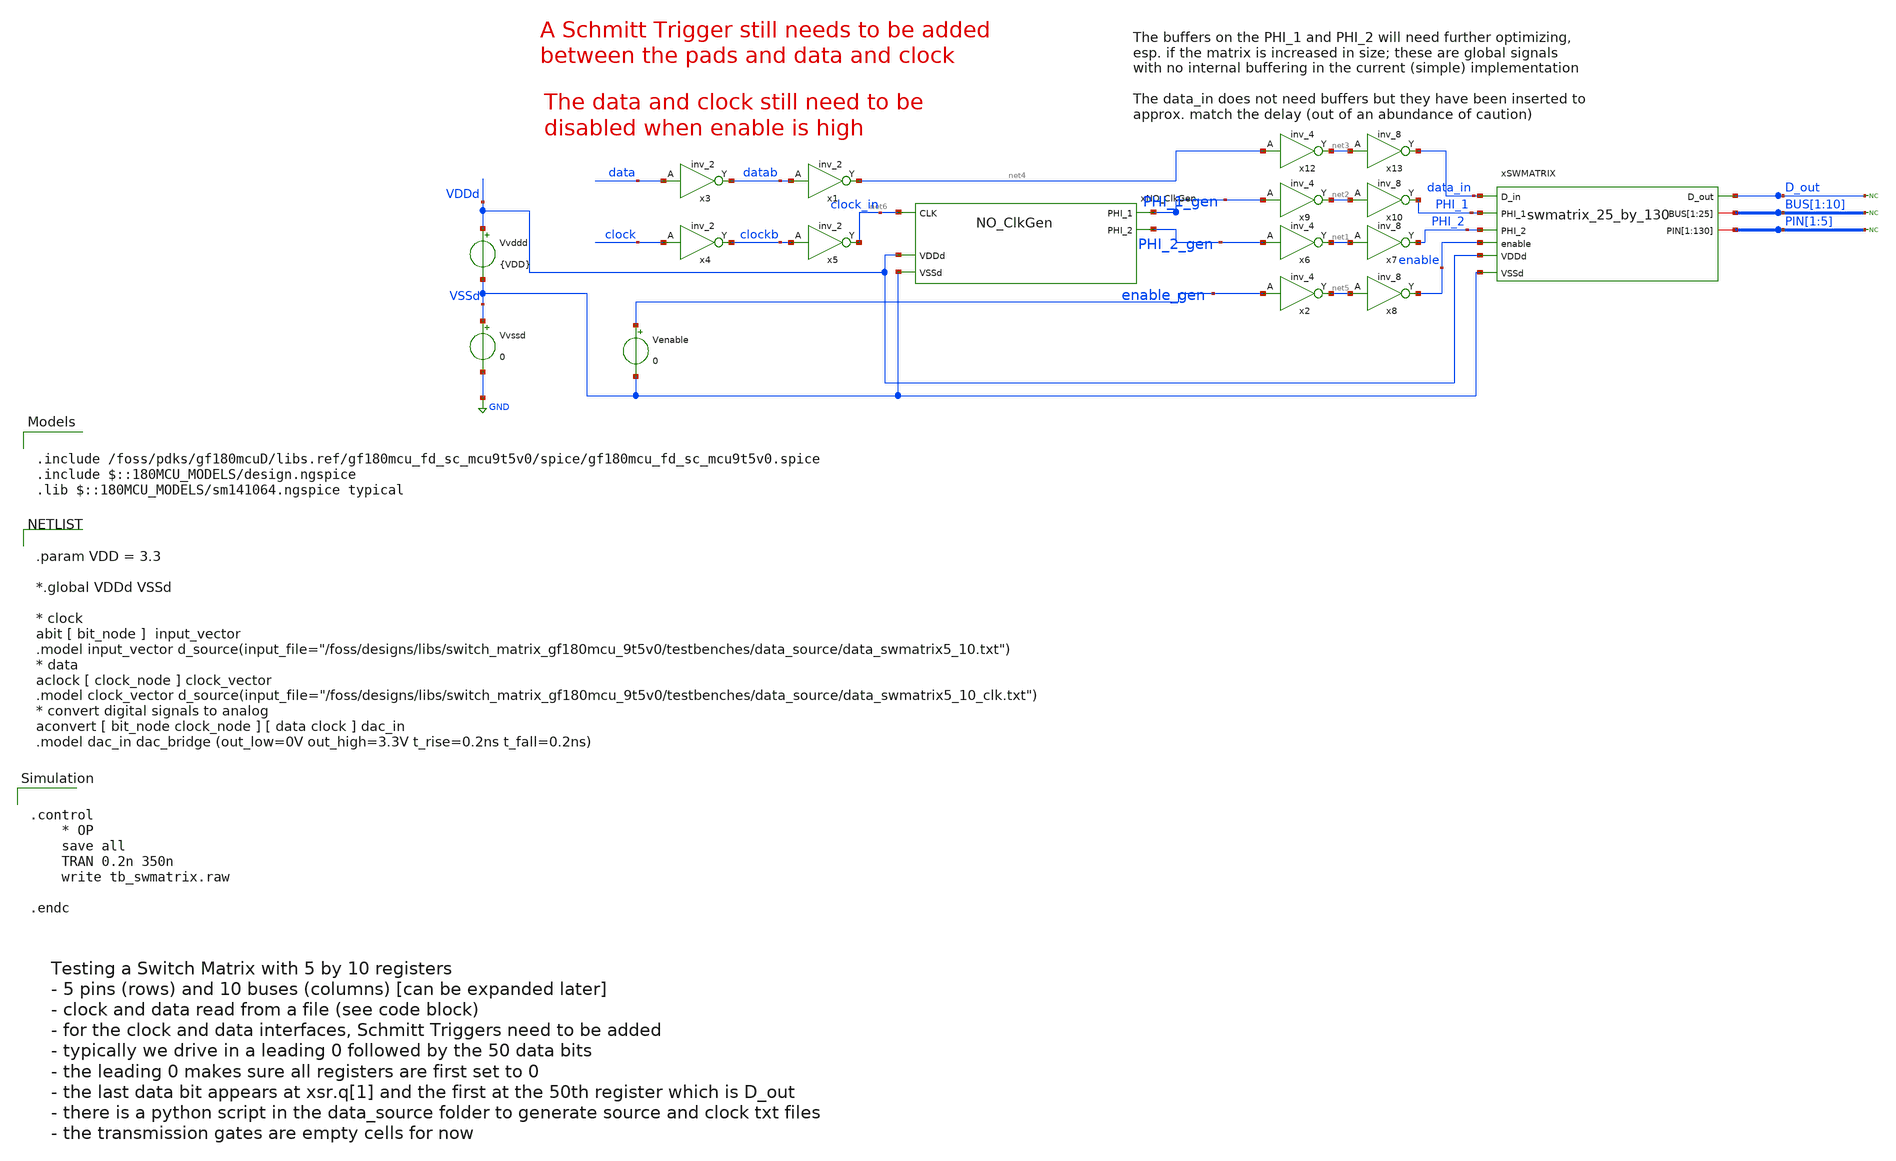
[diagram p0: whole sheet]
** sch_path: testbenches/tb_swmatrix_MOSbiusV3.sch
**.subckt tb_swmatrix_MOSbiusV3
Vvssd VSSd GND 0
Vvddd VDDd VSSd {VDD}
xNO_ClkGen PHI_2_gen net6 PHI_1_gen VDDd VSSd NO_ClkGen
x3 data VSSd VDDd VSSd VDDd datab gf180mcu_fd_sc_mcu9t5v0__inv_2
x1 datab VSSd VDDd VSSd VDDd net4 gf180mcu_fd_sc_mcu9t5v0__inv_2
x4 clock VSSd VDDd VSSd VDDd clockb gf180mcu_fd_sc_mcu9t5v0__inv_2
x5 clockb VSSd VDDd VSSd VDDd net6 gf180mcu_fd_sc_mcu9t5v0__inv_2
xSWMATRIX data_in D_out PHI_1 PHI_2 BUS[1] BUS[2] BUS[3] BUS[4] BUS[5] BUS[6] BUS[7] BUS[8] BUS[9]
+ BUS[10] BUS[1] BUS[2] BUS[3] BUS[4] BUS[5] BUS[6] BUS[7] BUS[8] BUS[9] BUS[10] BUS[1] BUS[2] BUS[3] BUS[4]
+ BUS[5] PIN[1] PIN[2] PIN[3] PIN[4] PIN[5] PIN[1] PIN[2] PIN[3] PIN[4] PIN[5] PIN[1] PIN[2] PIN[3] PIN[4]
+ PIN[5] PIN[1] PIN[2] PIN[3] PIN[4] PIN[5] PIN[1] PIN[2] PIN[3] PIN[4] PIN[5] PIN[1] PIN[2] PIN[3] PIN[4]
+ PIN[5] PIN[1] PIN[2] PIN[3] PIN[4] PIN[5] PIN[1] PIN[2] PIN[3] PIN[4] PIN[5] PIN[1] PIN[2] PIN[3] PIN[4]
+ PIN[5] PIN[1] PIN[2] PIN[3] PIN[4] PIN[5] PIN[1] PIN[2] PIN[3] PIN[4] PIN[5] PIN[1] PIN[2] PIN[3] PIN[4]
+ PIN[5] PIN[1] PIN[2] PIN[3] PIN[4] PIN[5] PIN[1] PIN[2] PIN[3] PIN[4] PIN[5] PIN[1] PIN[2] PIN[3] PIN[4]
+ PIN[5] PIN[1] PIN[2] PIN[3] PIN[4] PIN[5] PIN[1] PIN[2] PIN[3] PIN[4] PIN[5] PIN[1] PIN[2] PIN[3] PIN[4]
+ PIN[5] PIN[1] PIN[2] PIN[3] PIN[4] PIN[5] PIN[1] PIN[2] PIN[3] PIN[4] PIN[5] PIN[1] PIN[2] PIN[3] PIN[4]
+ PIN[5] PIN[1] PIN[2] PIN[3] PIN[4] PIN[5] PIN[1] PIN[2] PIN[3] PIN[4] PIN[5] PIN[1] PIN[2] PIN[3] PIN[4]
+ PIN[5] PIN[1] PIN[2] PIN[3] PIN[4] PIN[5] PIN[1] PIN[2] PIN[3] PIN[4] PIN[5] VDDd VSSd enable
+ swmatrix_25_by_130
* noconn D_out
* noconn BUS[1:10]
* noconn PIN[1:5]
x6 PHI_2_gen VSSd VDDd VSSd VDDd net1 gf180mcu_fd_sc_mcu9t5v0__inv_4
x7 net1 VSSd VDDd VSSd VDDd PHI_2 gf180mcu_fd_sc_mcu9t5v0__inv_8
x9 PHI_1_gen VSSd VDDd VSSd VDDd net2 gf180mcu_fd_sc_mcu9t5v0__inv_4
x10 net2 VSSd VDDd VSSd VDDd PHI_1 gf180mcu_fd_sc_mcu9t5v0__inv_8
x12 net4 VSSd VDDd VSSd VDDd net3 gf180mcu_fd_sc_mcu9t5v0__inv_4
x13 net3 VSSd VDDd VSSd VDDd data_in gf180mcu_fd_sc_mcu9t5v0__inv_8
x2 enable_gen VSSd VDDd VSSd VDDd net5 gf180mcu_fd_sc_mcu9t5v0__inv_4
x8 net5 VSSd VDDd VSSd VDDd enable gf180mcu_fd_sc_mcu9t5v0__inv_8
Venable enable_gen VSSd 0
**** begin user architecture code


.control
    * OP
    save all
    TRAN 0.2n 350n
    write tb_swmatrix.raw

.endc



.include /foss/pdks/gf180mcuD/libs.ref/gf180mcu_fd_sc_mcu9t5v0/spice/gf180mcu_fd_sc_mcu9t5v0.spice
.include $::180MCU_MODELS/design.ngspice
.lib $::180MCU_MODELS/sm141064.ngspice typical



.param VDD = 3.3

*.global VDDd VSSd

* clock
abit [ bit_node ]  input_vector
.model input_vector
+ d_source(input_file="/foss/designs/libs/switch_matrix_gf180mcu_9t5v0/testbenches/data_source/data_swmatrix5_10.txt")
* data
aclock [ clock_node ] clock_vector
.model clock_vector
+ d_source(input_file="/foss/designs/libs/switch_matrix_gf180mcu_9t5v0/testbenches/data_source/data_swmatrix5_10_clk.txt")
* convert digital signals to analog
aconvert [ bit_node clock_node ] [ data clock ] dac_in
.model dac_in dac_bridge (out_low=0V out_high=3.3V t_rise=0.2ns t_fall=0.2ns)


**** end user architecture code
**.ends
.GLOBAL GND
.end
